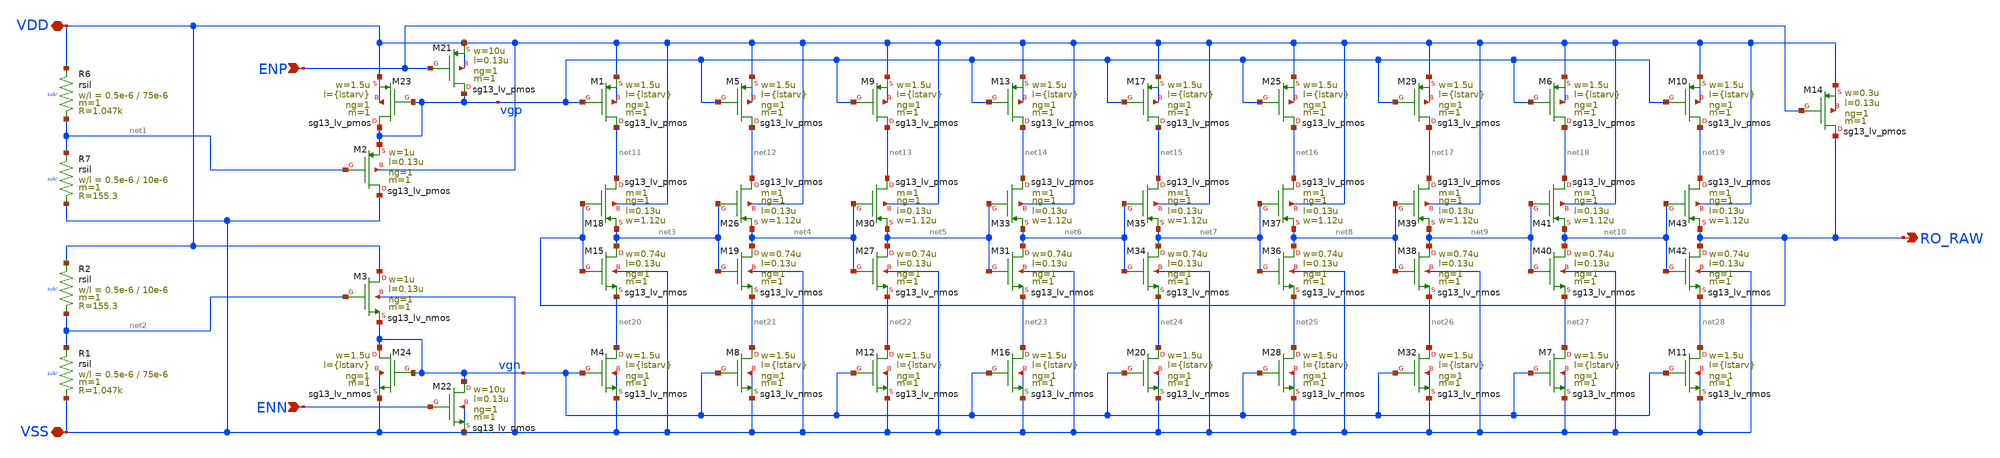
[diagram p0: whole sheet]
** sch_path: TSENSE8490-main/schematic/xschem/lvs-view/analog/temp-sens-core/temp_sens_core.sch
**.subckt temp_sens_core RO_RAW VDD VSS ENP ENN
*.opin RO_RAW
*.iopin VDD
*.iopin VSS
*.ipin ENP
*.ipin ENN
XM1 net11 vgp VDD VDD sg13_lv_pmos w=1.5u l={lstarv} ng=1 m=1 mm_ok=1
XM21 vgp ENP VDD VDD sg13_lv_pmos w=10u l=0.13u ng=1 m=1 mm_ok=1
XM22 vgn ENN VSS VSS sg13_lv_nmos w=10u l=0.13u ng=1 m=1 mm_ok=1
XM23 vgp vgp VDD VDD sg13_lv_pmos w=1.5u l={lstarv} ng=1 m=1 mm_ok=1
XM24 vgn vgn VSS VSS sg13_lv_nmos w=1.5u l={lstarv} ng=1 m=1 mm_ok=1
XM4 net20 vgn VSS VSS sg13_lv_nmos w=1.5u l={lstarv} ng=1 m=1 mm_ok=1
XM5 net12 vgp VDD VDD sg13_lv_pmos w=1.5u l={lstarv} ng=1 m=1 mm_ok=1
XM8 net21 vgn VSS VSS sg13_lv_nmos w=1.5u l={lstarv} ng=1 m=1 mm_ok=1
XM9 net13 vgp VDD VDD sg13_lv_pmos w=1.5u l={lstarv} ng=1 m=1 mm_ok=1
XM12 net22 vgn VSS VSS sg13_lv_nmos w=1.5u l={lstarv} ng=1 m=1 mm_ok=1
XM13 net14 vgp VDD VDD sg13_lv_pmos w=1.5u l={lstarv} ng=1 m=1 mm_ok=1
XM16 net23 vgn VSS VSS sg13_lv_nmos w=1.5u l={lstarv} ng=1 m=1 mm_ok=1
XM17 net15 vgp VDD VDD sg13_lv_pmos w=1.5u l={lstarv} ng=1 m=1 mm_ok=1
XM20 net24 vgn VSS VSS sg13_lv_nmos w=1.5u l={lstarv} ng=1 m=1 mm_ok=1
XM25 net16 vgp VDD VDD sg13_lv_pmos w=1.5u l={lstarv} ng=1 m=1 mm_ok=1
XM28 net25 vgn VSS VSS sg13_lv_nmos w=1.5u l={lstarv} ng=1 m=1 mm_ok=1
XM29 net17 vgp VDD VDD sg13_lv_pmos w=1.5u l={lstarv} ng=1 m=1 mm_ok=1
XM32 net26 vgn VSS VSS sg13_lv_nmos w=1.5u l={lstarv} ng=1 m=1 mm_ok=1
XM2 VSS net1 vgp VDD sg13_lv_pmos w=1u l=0.13u ng=1 m=1 mm_ok=1
XM3 VDD net2 vgn VSS sg13_lv_nmos w=1u l=0.13u ng=1 m=1 mm_ok=1
XR6 VDD net1 sub! rsil w=0.5e-6 l=75e-6 m=1 mm_ok=1
XR7 net1 VSS sub! rsil w=0.5e-6 l=10e-6 m=1 mm_ok=1
XR1 net2 VSS sub! rsil w=0.5e-6 l=75e-6 m=1 mm_ok=1
XR2 VDD net2 sub! rsil w=0.5e-6 l=10e-6 m=1 mm_ok=1
XM6 net18 vgp VDD VDD sg13_lv_pmos w=1.5u l={lstarv} ng=1 m=1 mm_ok=1
XM7 net27 vgn VSS VSS sg13_lv_nmos w=1.5u l={lstarv} ng=1 m=1 mm_ok=1
XM10 net19 vgp VDD VDD sg13_lv_pmos w=1.5u l={lstarv} ng=1 m=1 mm_ok=1
XM11 net28 vgn VSS VSS sg13_lv_nmos w=1.5u l={lstarv} ng=1 m=1 mm_ok=1
XM14 RO_RAW ENP VDD VDD sg13_lv_pmos w=0.3u l=0.13u ng=1 m=1 mm_ok=1
XM15 net3 RO_RAW net20 VSS sg13_lv_nmos w=0.74u l=0.13u ng=1 m=1 mm_ok=1
XM18 net11 RO_RAW net3 VDD sg13_lv_pmos w=1.12u l=0.13u ng=1 m=1 mm_ok=1
XM19 net4 net3 net21 VSS sg13_lv_nmos w=0.74u l=0.13u ng=1 m=1 mm_ok=1
XM26 net12 net3 net4 VDD sg13_lv_pmos w=1.12u l=0.13u ng=1 m=1 mm_ok=1
XM27 net5 net4 net22 VSS sg13_lv_nmos w=0.74u l=0.13u ng=1 m=1 mm_ok=1
XM30 net13 net4 net5 VDD sg13_lv_pmos w=1.12u l=0.13u ng=1 m=1 mm_ok=1
XM31 net6 net5 net23 VSS sg13_lv_nmos w=0.74u l=0.13u ng=1 m=1 mm_ok=1
XM33 net14 net5 net6 VDD sg13_lv_pmos w=1.12u l=0.13u ng=1 m=1 mm_ok=1
XM34 net7 net6 net24 VSS sg13_lv_nmos w=0.74u l=0.13u ng=1 m=1 mm_ok=1
XM35 net15 net6 net7 VDD sg13_lv_pmos w=1.12u l=0.13u ng=1 m=1 mm_ok=1
XM36 net8 net7 net25 VSS sg13_lv_nmos w=0.74u l=0.13u ng=1 m=1 mm_ok=1
XM37 net16 net7 net8 VDD sg13_lv_pmos w=1.12u l=0.13u ng=1 m=1 mm_ok=1
XM38 net9 net8 net26 VSS sg13_lv_nmos w=0.74u l=0.13u ng=1 m=1 mm_ok=1
XM39 net17 net8 net9 VDD sg13_lv_pmos w=1.12u l=0.13u ng=1 m=1 mm_ok=1
XM40 net10 net9 net27 VSS sg13_lv_nmos w=0.74u l=0.13u ng=1 m=1 mm_ok=1
XM41 net18 net9 net10 VDD sg13_lv_pmos w=1.12u l=0.13u ng=1 m=1 mm_ok=1
XM42 RO_RAW net10 net28 VSS sg13_lv_nmos w=0.74u l=0.13u ng=1 m=1 mm_ok=1
XM43 net19 net10 RO_RAW VDD sg13_lv_pmos w=1.12u l=0.13u ng=1 m=1 mm_ok=1
**.ends
.end
